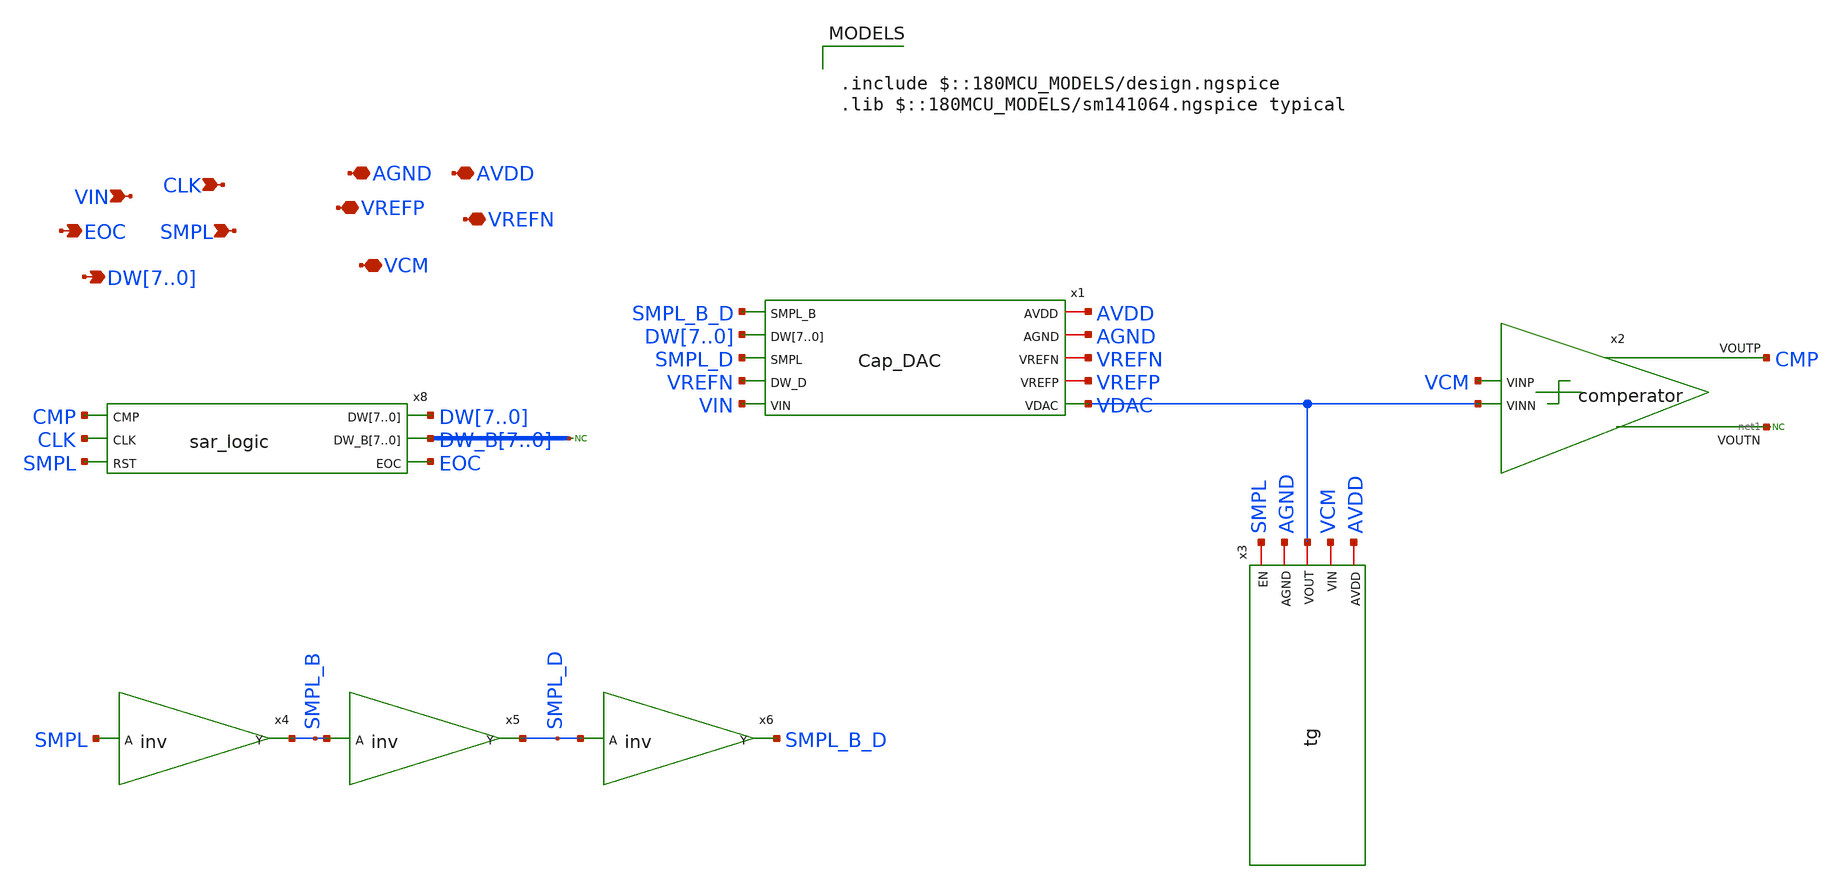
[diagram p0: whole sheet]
** sch_path: XSCHEM Files/SAR_DAC.sch
**.subckt SAR_DAC AGND AVDD VREFP VREFN VCM VIN SMPL CLK EOC DW7,DW6,DW5,DW4,DW3,DW2,DW1,DW0
*.iopin AGND
*.iopin AVDD
*.iopin VREFP
*.iopin VREFN
*.iopin VCM
*.ipin VIN
*.ipin SMPL
*.ipin CLK
*.opin EOC
*.opin DW7,DW6,DW5,DW4,DW3,DW2,DW1,DW0
* noconn DW_B[7..0]
* noconn #net1
x8 CMP CLK SMPL DW7 DW6 DW5 DW4 DW3 DW2 DW1 DW0 DW_B7 DW_B6 DW_B5 DW_B4 DW_B3 DW_B2 DW_B1 DW_B0 EOC
+ sar_logic
x2 CMP VCM net1 VDAC comperator
x4 SMPL_B SMPL inv
x5 SMPL_D SMPL_B inv
x6 SMPL_B_D SMPL_D inv
x1 AVDD AGND VREFN VREFP SMPL_B_D DW7 DW6 DW5 DW4 DW3 DW2 DW1 DW0 SMPL_D VREFN VIN VDAC Cap_DAC
x3 SMPL AGND VDAC VCM AVDD tg
**** begin user architecture code

.include $::180MCU_MODELS/design.ngspice
.lib $::180MCU_MODELS/sm141064.ngspice typical

**** end user architecture code
**.ends

* expanding   symbol:  /home/tare/Desktop/Final_1/sar_logic.sym # of pins=6
** sym_path: XSCHEM Files/sar_logic.sym
** sch_path: XSCHEM Files/sar_logic.sch
.subckt sar_logic CMP CLK RST DW7 DW6 DW5 DW4 DW3 DW2 DW1 DW0 DW_B7 DW_B6 DW_B5 DW_B4 DW_B3 DW_B2
+ DW_B1 DW_B0 EOC
*.ipin CMP
*.opin DW7,DW6,DW5,DW4,DW3,DW2,DW1,DW0
*.ipin CLK
*.ipin RST
*.opin DW_B7,DW_B6,DW_B5,DW_B4,DW_B3,DW_B2,DW_B1,DW_B0
*.opin EOC
**** begin user architecture code


V1 VLOW 0 0


**** end user architecture code
xRING_CNT8 VLOW CLK RST VLOW QCNT8 Q_B8 dff
xRING_CNT7 QCNT8 CLK VLOW RST QCNT7 Q_B7 dff
xRING_CNT6 QCNT7 CLK VLOW RST QCNT6 Q_B6 dff
xRING_CNT5 QCNT6 CLK VLOW RST QCNT5 Q_B5 dff
xRING_CNT4 QCNT5 CLK VLOW RST QCNT4 Q_B4 dff
xRING_CNT3 QCNT4 CLK VLOW RST QCNT3 Q_B3 dff
xRING_CNT2 QCNT3 CLK VLOW RST QCNT2 Q_B2 dff
xRING_CNT1 QCNT2 CLK VLOW RST QCNT1 Q_B1 dff
xRING_CNT0 QCNT1 CLK VLOW RST QCNT0 Q_B0 dff
xCODE_REG7 CMP DW6 QCNT8 VLOW DW7 DW_B7 dff
xCODE_REG6 CMP DW5 QCNT7 RST DW6 DW_B6 dff
xCODE_REG5 CMP DW4 QCNT6 RST DW5 DW_B5 dff
xCODE_REG4 CMP DW3 QCNT5 RST DW4 DW_B4 dff
xCODE_REG3 CMP DW2 QCNT4 RST DW3 DW_B3 dff
xCODE_REG2 CMP DW1 QCNT3 RST DW2 DW_B2 dff
xCODE_REG1 CMP DW0 QCNT2 RST DW1 DW_B1 dff
xCODE_REG0 CMP EOC QCNT1 RST DW0 DW_B0 dff
x3 VLOW VLOW QCNT0 RST EOC net1 dff
.ends


* expanding   symbol:  /home/tare/Desktop/Final_1/comperator.sym # of pins=4
** sym_path: XSCHEM Files/comperator.sym
** sch_path: XSCHEM Files/comperator.sch
.subckt comperator VOUTP VINP VOUTN VINN
*.ipin VINP
*.opin VOUTP
*.ipin VINN
*.opin VOUTN
V1 VINPi VINP 0
V2 VINNi VINN 0
B2 VOUTN GND V = {VCC/2 + VCC/2 *(tanh(V(VINPi,VINNi)*1e6*-1))}
B1 VOUTP GND V = {VCC/2 + VCC/2 *(tanh(V(VINPi,VINNi)*1e6))}
.ends


* expanding   symbol:  /home/tare/Desktop/Final_1/inv.sym # of pins=2
** sym_path: XSCHEM Files/inv.sym
** sch_path: XSCHEM Files/inv.sch
.subckt inv Y A
*.ipin A
*.opin Y
**** begin user architecture code


*inverter model
a1 A Yi my_inv
.model my_inv d_inverter(rise_delay = 1e-9 fall_delay = 1e-9                         input_load =
+ 1e-12)

*force netlisting of digital outputs
v1 Yi Y 0


**** end user architecture code
.ends


* expanding   symbol:  /home/tare/Desktop/last/Cap_DAC.sym # of pins=10
** sym_path: XSCHEM Files/Cap_DAC.sym
** sch_path: XSCHEM Files/Cap_DAC.sch
.subckt Cap_DAC AVDD AGND VREFN VREFP SMPL_B DW7 DW6 DW5 DW4 DW3 DW2 DW1 DW0 SMPL DW_D VIN VDAC
*.iopin AVDD
*.iopin VREFP
*.iopin VREFN
*.ipin VIN
*.ipin SMPL_B
*.ipin SMPL
*.opin VDAC
*.ipin DW7,DW6,DW5,DW4,DW3,DW2,DW1,DW0
*.ipin DW_D
*.iopin AGND
C0 VDAC VBOT_D 1f m=1
C1 VDAC VBOT0 1f m=1
C2 VDAC VBOT1 1f m=2
C3 VDAC VBOT2 1f m=4
C4 VDAC VBOT3 1f m=8
C5 VDAC VBOT4 1f m=16
C6 VDAC VBOT5 1f m=32
C7 VDAC VBOT6 1f m=64
C8 VDAC VBOT7 1f m=128
x17 VREFN VREFP AGND AVDD VIN DW7 SMPL SMPL_B VBOT7 Bottom_Plate
x16 VREFN VREFP AGND AVDD VIN DW6 SMPL SMPL_B VBOT6 Bottom_Plate
x15 VREFN VREFP AGND AVDD VIN DW5 SMPL SMPL_B VBOT5 Bottom_Plate
x14 VREFN VREFP AGND AVDD VIN DW4 SMPL SMPL_B VBOT4 Bottom_Plate
x13 VREFN VREFP AGND AVDD VIN DW3 SMPL SMPL_B VBOT3 Bottom_Plate
x12 VREFN VREFP AGND AVDD VIN DW2 SMPL SMPL_B VBOT2 Bottom_Plate
x11 VREFN VREFP AGND AVDD VIN DW1 SMPL SMPL_B VBOT1 Bottom_Plate
x10 VREFN VREFP AGND AVDD VIN DW0 SMPL SMPL_B VBOT0 Bottom_Plate
x2 VREFN VREFP AGND AVDD VIN DW_D SMPL SMPL_B VBOT_D Bottom_Plate
.ends


* expanding   symbol:  /home/tare/Desktop/last/tg.sym # of pins=5
** sym_path: XSCHEM Files/tg.sym
** sch_path: XSCHEM Files/tg.sch
.subckt tg EN AGND VOUT VIN AVDD
*.iopin AGND
*.iopin AVDD
*.iopin VOUT
*.iopin VIN
*.iopin EN
XM1 VOUT EN VIN AGND nmos_3p3 L=0.28u W=5u nf=1 ad='int((nf+1)/2) * W/nf * 0.18u' as='int((nf+2)/2) * W/nf * 0.18u'
+ pd='2*int((nf+1)/2) * (W/nf + 0.18u)' ps='2*int((nf+2)/2) * (W/nf + 0.18u)' nrd='0.18u / W' nrs='0.18u / W'
+ sa=0 sb=0 sd=0 m=1
XM2 VOUT ENB VIN AVDD pmos_3p3 L=0.28u W=10u nf=1 ad='int((nf+1)/2) * W/nf * 0.18u' as='int((nf+2)/2) * W/nf * 0.18u'
+ pd='2*int((nf+1)/2) * (W/nf + 0.18u)' ps='2*int((nf+2)/2) * (W/nf + 0.18u)' nrd='0.18u / W' nrs='0.18u / W'
+ sa=0 sb=0 sd=0 m=1
E1 ENB AVDD EN AGND -1
.ends


* expanding   symbol:  /home/tare/Desktop/sar_adc/dff.sym # of pins=6
** sym_path: XSCHEM Files/dff.sym
** sch_path: XSCHEM Files/dff.sch
.subckt dff D CLK SET RESET Q QB
*.ipin D
*.opin Q
*.ipin CLK
*.ipin SET
*.ipin RESET
*.opin QB
**** begin user architecture code


*nor model
a1 D CLK SET RESET OUT OUTI my_dff
.model my_dff d_dff(clk_delay = 13.0e-9 set_delay = 25.0e-9                    reset_delay = 27.0e-9
+ ic = 2 rise_delay = 10.0e-9                    fall_delay = 3e-9)

*force netlisting of digital outputs
v1 OUT Q 0
v2 OUTI QB 1


**** end user architecture code
.ends


* expanding   symbol:  /home/tare/Desktop/last/Bottom_Plate.sym # of pins=9
** sym_path: XSCHEM Files/Bottom_Plate.sym
** sch_path: XSCHEM Files/Bottom_Plate.sch
.subckt Bottom_Plate VREFN VREFP AGND AVDD VIN D SMPL SMPL_B VBOT
*.iopin AGND
*.iopin AVDD
*.iopin VREFP
*.iopin VREFN
*.opin VBOT
*.ipin VIN
*.ipin D
*.ipin SMPL_B
*.ipin SMPL
XM1 VBOT net1 VREFN AGND nmos_3p3 L=0.28u W=5u nf=1 ad='int((nf+1)/2) * W/nf * 0.18u' as='int((nf+2)/2) * W/nf * 0.18u'
+ pd='2*int((nf+1)/2) * (W/nf + 0.18u)' ps='2*int((nf+2)/2) * (W/nf + 0.18u)' nrd='0.18u / W' nrs='0.18u / W'
+ sa=0 sb=0 sd=0 m=1
XM2 VREFP net2 VBOT AVDD pmos_3p3 L=0.28u W=10u nf=1 ad='int((nf+1)/2) * W/nf * 0.18u' as='int((nf+2)/2) * W/nf * 0.18u'
+ pd='2*int((nf+1)/2) * (W/nf + 0.18u)' ps='2*int((nf+2)/2) * (W/nf + 0.18u)' nrd='0.18u / W' nrs='0.18u / W'
+ sa=0 sb=0 sd=0 m=1
x2 net1 D SMPL nor
x3 net2 D SMPL_B nand
x1 SMPL AGND VBOT VIN AVDD tg
.ends


* expanding   symbol:  /home/tare/Desktop/Final_1/nor.sym # of pins=3
** sym_path: XSCHEM Files/nor.sym
** sch_path: XSCHEM Files/nor.sch
.subckt nor Y A B
*.ipin A
*.opin Y
*.ipin B
**** begin user architecture code


*nor model
a1 [A b] Yi my_nor
.model my_nor d_nor(rise_delay = 1e-9 fall_delay = 1e-9                         input_load = 1e-12)

*force netlisting of digital outputs
v1 Yi Y 0


**** end user architecture code
.ends


* expanding   symbol:  /home/tare/Desktop/Final_1/nand.sym # of pins=3
** sym_path: XSCHEM Files/nand.sym
** sch_path: XSCHEM Files/nand.sch
.subckt nand Y A B
*.ipin A
*.opin Y
*.ipin B
**** begin user architecture code


*nand model
a1 [A b] Yi my_nand
.model my_nand d_nand(rise_delay = 1e-9 fall_delay = 1e-9                         input_load =
+ 1e-12)

*force netlisting of digital outputs
v1 Yi Y 0


**** end user architecture code
.ends

.GLOBAL GND
.end
